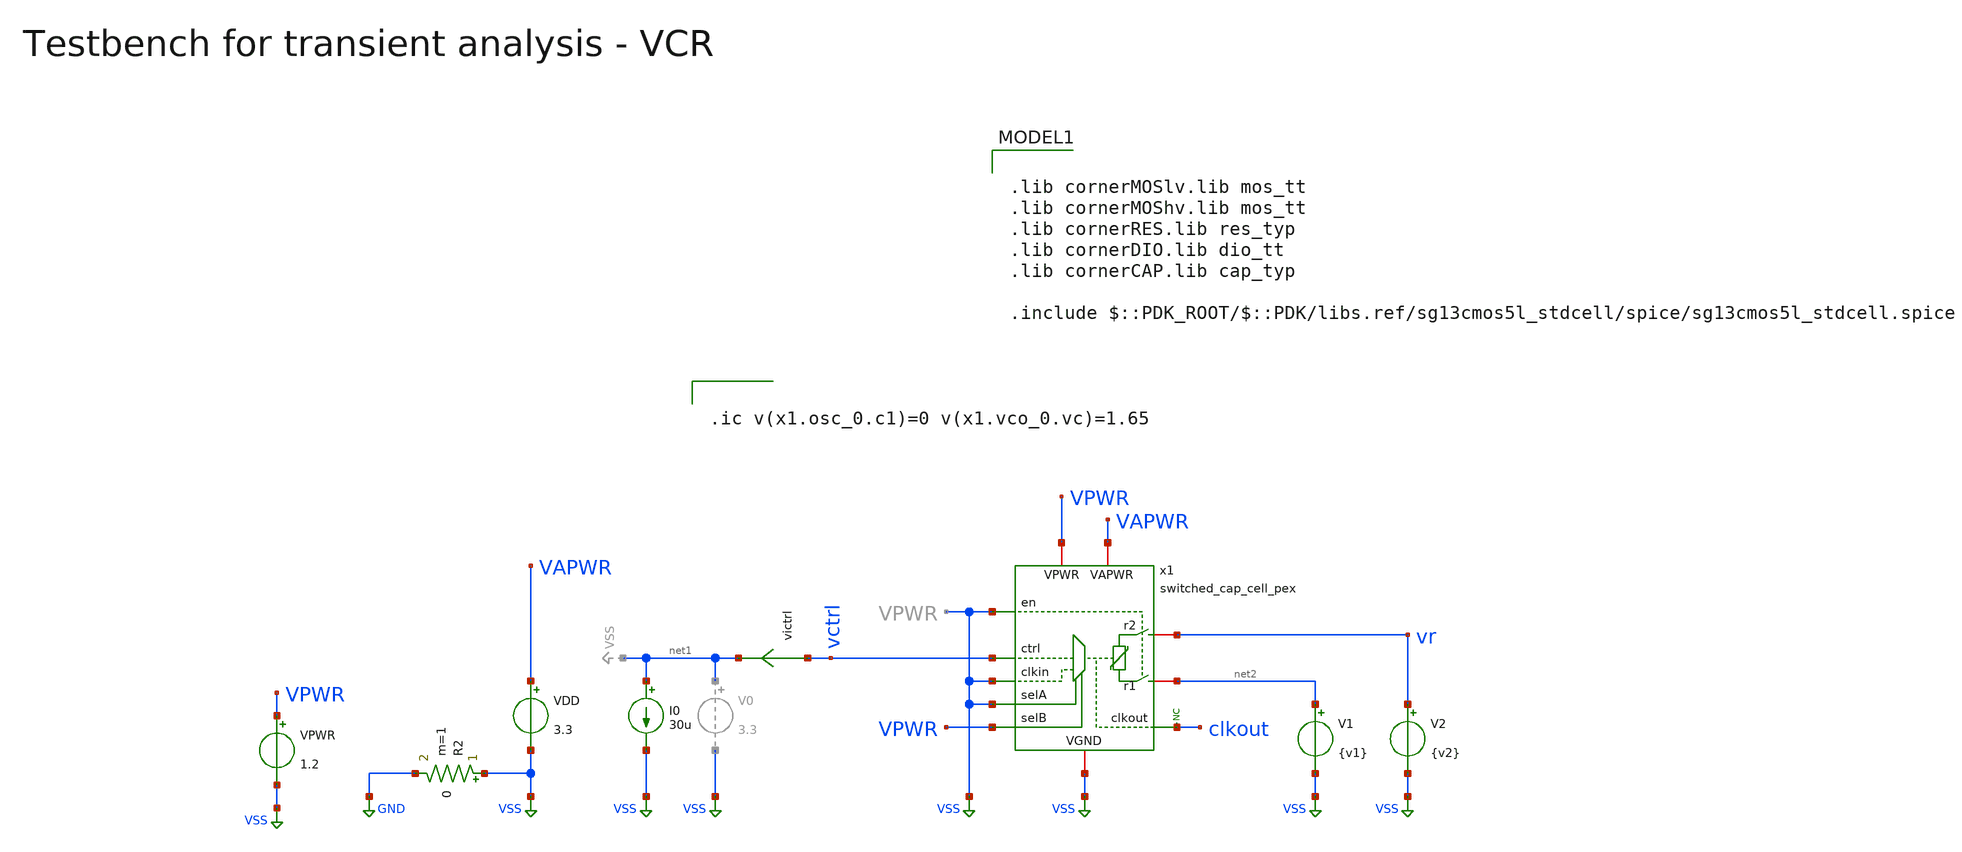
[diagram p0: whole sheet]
** sch_path: macros/heichips26_vcr/macros/switched_capacitor/testbenches/xschem/tb_switched_cap_pex_tran.sch
**.subckt tb_switched_cap_pex_tran
VDD VAPWR VSS 3.3
R2 VSS GND 0 m=1
I0 net1 VSS 30u
V1 net2 VSS {v1}
V2 vr VSS {v2}
VPWR VPWR VSS 1.2
* noconn clkout
x1 vctrl VAPWR VSS vr net2 VSS VSS VPWR VSS VPWR clkout switched_cap_cell_pex
victrl vctrl net1 0
.save i(victrl)
**** begin user architecture code

.lib cornerMOSlv.lib mos_tt
.lib cornerMOShv.lib mos_tt
.lib cornerRES.lib res_typ
.lib cornerDIO.lib dio_tt
.lib cornerCAP.lib cap_typ

.include $::PDK_ROOT/$::PDK/libs.ref/sg13cmos5l_stdcell/spice/sg13cmos5l_stdcell.spice



.include ../../../netlist/pex/switched_cap_cell_magic_pex_1_manual_caps.spice

.param temp=27
.param vctrl  = 0.1
*.param f      = {2e6/vctrl}
.param f = 10Meg

* Derived timing parameters
.param period = {1/f}
.param ton    = {period/2}
.csparam tstop  = {5*period}
.csparam tstep  = {period/100}
.param ictrl  = {f*3.3e-12}
.param tr     = {period/1000}
.param tf     = {period/1000}

.param VDD = 3.3
.csparam VDD=VDD
.param vdm = 3.3
.param vcm = {VDD/2}
.param v1  = {vcm - vdm/2}
.param v2  = {vcm + vdm/2}

.options savecurrents klu method=gear reltol=1e-6 abstol=1e-12 gmin=1e-15
.probe alli
.control

save all
set appendwrite

tran {$&tstep} {$&tstop}
remzerovec

save all
set appendwrite

write @schname\.raw
set appendwrite

*let r_var = vr/i(r1)
meas tran period_sim TRIG i(V1) VAL=1m RISE=1 TARG i(V1) VAL=1m RISE=2
meas tran n_periods TRIG i(V1) VAL=1m RISE=1 TARG i(V1) VAL=1m RISE=LAST
meas tran i_avg AVG i(V1) FROM=0 TO=n_periods
meas tran v_avg AVG vr FROM=0 TO=n_periods
*meas tran r_avg AVG r_var

let npts = length(time) - 1
let i_mavg = integ(i(V1))[1, npts] / time[1, npts]
let v_mavg = integ(vr)[1, npts] / time[1, npts]
let r_mavg = v_mavg/i_mavg
let r_avg = v_avg/i_avg
let f_sim = 1/period_sim
let plot_y_lim = 1.2*r_avg

print period_sim f_sim r_avg

* Plotting
*plot vr v_avg v_mavg
plot i(V1) i_avg i_mavg
plot r_avg r_mavg ylimit 0 $&plot_y_lim
plot clkout
plot i(victrl) mean(i(victrl))
plot vctrl

* Write Data
unset appendwrite
set wr_vecnames
set wr_singlescale
wrdata ../plot_simulations/data/@schname\.txt v(vr) v(VDD) i(V1)

*quit
.endc




.ic v(x1.osc_0.c1)=0 v(x1.vco_0.vc)=1.65


**** end user architecture code
**.ends
.GLOBAL VSS
.GLOBAL GND
.end
